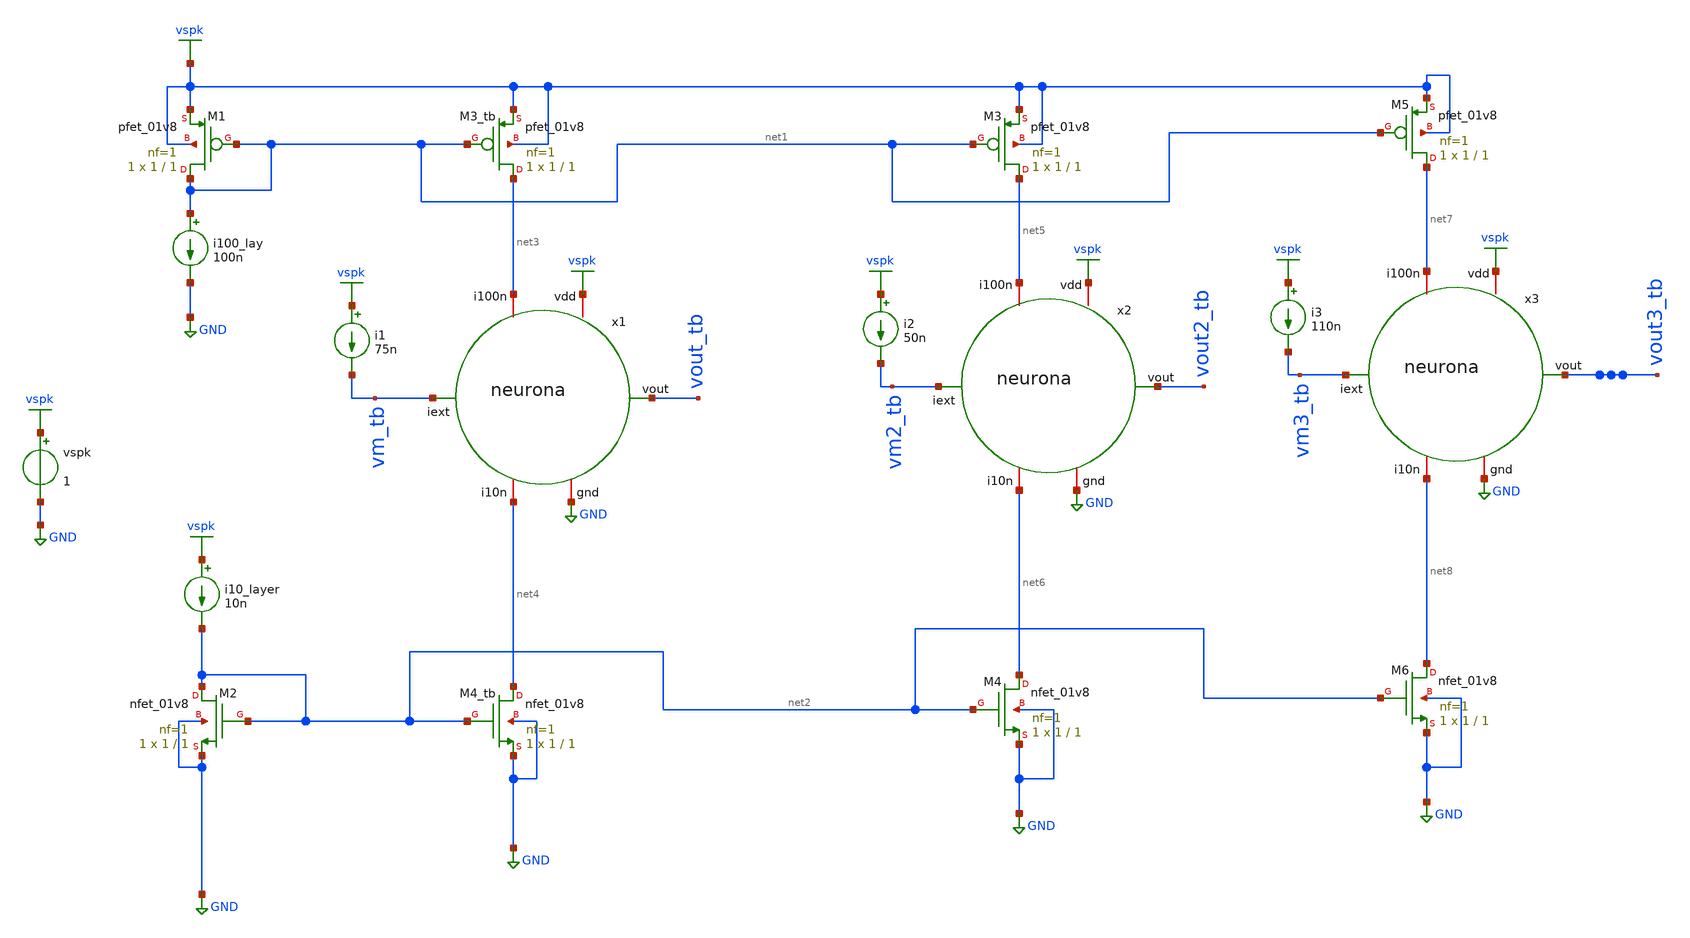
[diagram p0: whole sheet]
** sch_path: Neuron/ultralif/layer.sch
**.subckt layer
XM1 net1 net1 vspk vspk sky130_fd_pr__pfet_01v8 L=1 W=1 nf=1 ad='int((nf+1)/2) * W/nf * 0.29' as='int((nf+2)/2) * W/nf * 0.29'
+ pd='2*int((nf+1)/2) * (W/nf + 0.29)' ps='2*int((nf+2)/2) * (W/nf + 0.29)' nrd='0.29 / W' nrs='0.29 / W'
+ sa=0 sb=0 sd=0 mult=1 m=1
i100_lay net1 GND 100n
XM2 net2 net2 GND GND sky130_fd_pr__nfet_01v8 L=1 W=1 nf=1 ad='int((nf+1)/2) * W/nf * 0.29' as='int((nf+2)/2) * W/nf * 0.29'
+ pd='2*int((nf+1)/2) * (W/nf + 0.29)' ps='2*int((nf+2)/2) * (W/nf + 0.29)' nrd='0.29 / W' nrs='0.29 / W'
+ sa=0 sb=0 sd=0 mult=1 m=1
i10_layer vspk net2 10n
vspk vspk GND 1
XM3_tb net3 net1 vspk vspk sky130_fd_pr__pfet_01v8 L=1 W=1 nf=1 ad='int((nf+1)/2) * W/nf * 0.29' as='int((nf+2)/2) * W/nf * 0.29'
+ pd='2*int((nf+1)/2) * (W/nf + 0.29)' ps='2*int((nf+2)/2) * (W/nf + 0.29)' nrd='0.29 / W' nrs='0.29 / W'
+ sa=0 sb=0 sd=0 mult=1 m=1
XM4_tb net4 net2 GND GND sky130_fd_pr__nfet_01v8 L=1 W=1 nf=1 ad='int((nf+1)/2) * W/nf * 0.29' as='int((nf+2)/2) * W/nf * 0.29'
+ pd='2*int((nf+1)/2) * (W/nf + 0.29)' ps='2*int((nf+2)/2) * (W/nf + 0.29)' nrd='0.29 / W' nrs='0.29 / W'
+ sa=0 sb=0 sd=0 mult=1 m=1
x1 vspk net3 vm_tb vout_tb net4 GND neurona
i1 vspk vm_tb 75n
x2 vspk net5 vm2_tb vout2_tb net6 GND neurona
XM3 net5 net1 vspk vspk sky130_fd_pr__pfet_01v8 L=1 W=1 nf=1 ad='int((nf+1)/2) * W/nf * 0.29' as='int((nf+2)/2) * W/nf * 0.29'
+ pd='2*int((nf+1)/2) * (W/nf + 0.29)' ps='2*int((nf+2)/2) * (W/nf + 0.29)' nrd='0.29 / W' nrs='0.29 / W'
+ sa=0 sb=0 sd=0 mult=1 m=1
i2 vspk vm2_tb 50n
XM4 net6 net2 GND GND sky130_fd_pr__nfet_01v8 L=1 W=1 nf=1 ad='int((nf+1)/2) * W/nf * 0.29' as='int((nf+2)/2) * W/nf * 0.29'
+ pd='2*int((nf+1)/2) * (W/nf + 0.29)' ps='2*int((nf+2)/2) * (W/nf + 0.29)' nrd='0.29 / W' nrs='0.29 / W'
+ sa=0 sb=0 sd=0 mult=1 m=1
x3 vspk net7 vm3_tb vout3_tb net8 GND neurona
XM5 net7 net1 vspk vspk sky130_fd_pr__pfet_01v8 L=1 W=1 nf=1 ad='int((nf+1)/2) * W/nf * 0.29' as='int((nf+2)/2) * W/nf * 0.29'
+ pd='2*int((nf+1)/2) * (W/nf + 0.29)' ps='2*int((nf+2)/2) * (W/nf + 0.29)' nrd='0.29 / W' nrs='0.29 / W'
+ sa=0 sb=0 sd=0 mult=1 m=1
i3 vspk vm3_tb 110n
XM6 net8 net2 GND GND sky130_fd_pr__nfet_01v8 L=1 W=1 nf=1 ad='int((nf+1)/2) * W/nf * 0.29' as='int((nf+2)/2) * W/nf * 0.29'
+ pd='2*int((nf+1)/2) * (W/nf + 0.29)' ps='2*int((nf+2)/2) * (W/nf + 0.29)' nrd='0.29 / W' nrs='0.29 / W'
+ sa=0 sb=0 sd=0 mult=1 m=1
**** begin user architecture code
.lib $::SKYWATER_MODELS/sky130.lib.spice tt
**** end user architecture code
**.ends

* expanding   symbol:  neurona.sym # of pins=6
** sym_path: Neuron/neurona.sym
** sch_path: Neuron/neurona.sch
.subckt neurona vdd i100n iext vout i10n gnd
*.ipin iext
*.iopin i10n
*.iopin gnd
*.iopin vdd
*.opin vout
*.iopin i100n
XM1 i10n i10n iext iext sky130_fd_pr__pfet_01v8 L=10 W=1 nf=1 ad='int((nf+1)/2) * W/nf * 0.29' as='int((nf+2)/2) * W/nf * 0.29'
+ pd='2*int((nf+1)/2) * (W/nf + 0.29)' ps='2*int((nf+2)/2) * (W/nf + 0.29)' nrd='0.29 / W' nrs='0.29 / W'
+ sa=0 sb=0 sd=0 mult=1 m=1
XM2 i10n net1 iext iext sky130_fd_pr__pfet_01v8 L=1 W=10 nf=1 ad='int((nf+1)/2) * W/nf * 0.29' as='int((nf+2)/2) * W/nf * 0.29'
+ pd='2*int((nf+1)/2) * (W/nf + 0.29)' ps='2*int((nf+2)/2) * (W/nf + 0.29)' nrd='0.29 / W' nrs='0.29 / W'
+ sa=0 sb=0 sd=0 mult=1 m=1
XM3 net1 net1 iext iext sky130_fd_pr__pfet_01v8 L=1 W=50 nf=1 ad='int((nf+1)/2) * W/nf * 0.29' as='int((nf+2)/2) * W/nf * 0.29'
+ pd='2*int((nf+1)/2) * (W/nf + 0.29)' ps='2*int((nf+2)/2) * (W/nf + 0.29)' nrd='0.29 / W' nrs='0.29 / W'
+ sa=0 sb=0 sd=0 mult=2 m=2
XM4 net1 i10n gnd gnd sky130_fd_pr__nfet_01v8 L=1 W=1 nf=1 ad='int((1 + 1)/2) * 1 / 1 * 0.29' as='int((1 + 2)/2) * 1 / 1 * 0.29'
+ pd='2*int((1 + 1)/2) * (1 / 1 + 0.29)' ps='2*int((1 + 2)/2) * (1 / 1 + 0.29)' nrd='0.29 / 1 ' nrs='0.29 / 1 '
+ sa=0 sb=0 sd=0 mult=1 m=1
XM5 i100n i10n gnd gnd sky130_fd_pr__nfet_01v8 L=1 W=1 nf=1 ad='int((1 + 1)/2) * 1 / 1 * 0.29' as='int((1 + 2)/2) * 1 / 1 * 0.29'
+ pd='2*int((1 + 1)/2) * (1 / 1 + 0.29)' ps='2*int((1 + 2)/2) * (1 / 1 + 0.29)' nrd='0.29 / 1 ' nrs='0.29 / 1 '
+ sa=0 sb=0 sd=0 mult=1 m=1
XM6 vout i100n vdd vdd sky130_fd_pr__pfet_01v8 L=1 W=1 nf=1 ad='int((nf+1)/2) * W/nf * 0.29' as='int((nf+2)/2) * W/nf * 0.29'
+ pd='2*int((nf+1)/2) * (W/nf + 0.29)' ps='2*int((nf+2)/2) * (W/nf + 0.29)' nrd='0.29 / W' nrs='0.29 / W'
+ sa=0 sb=0 sd=0 mult=1 m=1
XM7 vout i100n gnd gnd sky130_fd_pr__nfet_01v8 L=1 W=1 nf=1 ad='int((1 + 1)/2) * 1 / 1 * 0.29' as='int((1 + 2)/2) * 1 / 1 * 0.29'
+ pd='2*int((1 + 1)/2) * (1 / 1 + 0.29)' ps='2*int((1 + 2)/2) * (1 / 1 + 0.29)' nrd='0.29 / 1 ' nrs='0.29 / 1 '
+ sa=0 sb=0 sd=0 mult=1 m=1
C1 iext gnd 10p m=1
.ends

.GLOBAL GND
.GLOBAL vspk
**** begin user architecture code


.options savecurrents
.tran 50n 2m uic
.save all
.control
	run
	write layer_10.raw
*plot all.Vout
.endc


**** end user architecture code
.end
